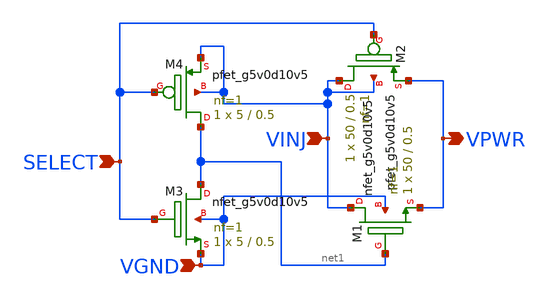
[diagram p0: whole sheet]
** sch_path: sky130_cells/ChargePump/InjectionTgate.sch
**.subckt InjectionTgate SELECT VGND VINJ VPWR
*.ipin SELECT
*.ipin VGND
*.ipin VINJ
*.opin VPWR
XM4 net1 SELECT VINJ VINJ sky130_fd_pr__pfet_g5v0d10v5 L=0.5 W=5 nf=1 ad='int((1 + 1)/2) * 5 / 1 * 0.29'
+ as='int((1 + 2)/2) * 5 / 1 * 0.29' pd='2*int((1 + 1)/2) * (5 / 1 + 0.29)' ps='2*int((1 + 2)/2) * (5 / 1 + 0.29)'
+ nrd='0.29 / 5 ' nrs='0.29 / 5 ' sa=0 sb=0 sd=0 mult=1 m=1
XM2 VINJ SELECT VPWR VINJ sky130_fd_pr__pfet_g5v0d10v5 L=0.5 W=50 nf=1 ad='int((1 + 1)/2) * 50 / 1 * 0.29'
+ as='int((1 + 2)/2) * 50 / 1 * 0.29' pd='2*int((1 + 1)/2) * (50 / 1 + 0.29)' ps='2*int((1 + 2)/2) * (50 / 1 + 0.29)'
+ nrd='0.29 / 50 ' nrs='0.29 / 50 ' sa=0 sb=0 sd=0 mult=1 m=1
XM3 net1 SELECT VGND VGND sky130_fd_pr__nfet_g5v0d10v5 L=0.5 W=5 nf=1 ad='int((1 + 1)/2) * 5 / 1 * 0.29'
+ as='int((1 + 2)/2) * 5 / 1 * 0.29' pd='2*int((1 + 1)/2) * (5 / 1 + 0.29)' ps='2*int((1 + 2)/2) * (5 / 1 + 0.29)'
+ nrd='0.29 / 5 ' nrs='0.29 / 5 ' sa=0 sb=0 sd=0 mult=1 m=1
XM1 VINJ net1 VPWR VGND sky130_fd_pr__nfet_g5v0d10v5 L=0.5 W=50 nf=1 ad='int((1 + 1)/2) * 50 / 1 * 0.29'
+ as='int((1 + 2)/2) * 50 / 1 * 0.29' pd='2*int((1 + 1)/2) * (50 / 1 + 0.29)' ps='2*int((1 + 2)/2) * (50 / 1 + 0.29)'
+ nrd='0.29 / 50 ' nrs='0.29 / 50 ' sa=0 sb=0 sd=0 mult=1 m=1
**.ends
.end
